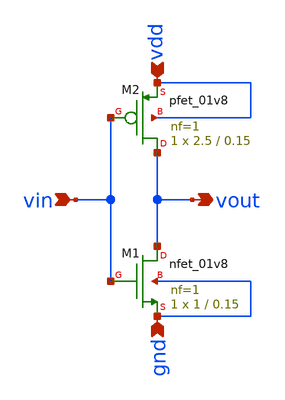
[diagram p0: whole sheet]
** sch_path: schematic/cmos_inverter.sch
**.subckt cmos_inverter vin vdd gnd vout
*.ipin vin
*.ipin vdd
*.ipin gnd
*.opin vout
XM1 vout vin gnd gnd sky130_fd_pr__nfet_01v8 L=0.15 W=1 nf=1 ad='int((1 + 1)/2) * 1 / 1 * 0.29' as='int((1 + 2)/2) * 1 / 1 * 0.29'
+ pd='2*int((1 + 1)/2) * (1 / 1 + 0.29)' ps='2*int((1 + 2)/2) * (1 / 1 + 0.29)' nrd='0.29 / 1 ' nrs='0.29 / 1 '
+ sa=0 sb=0 sd=0 mult=1 m=1
XM2 vout vin vdd vdd sky130_fd_pr__pfet_01v8 L=0.15 W=2.5 nf=1 ad='int((1 + 1)/2) * 2.5 / 1 * 0.29' as='int((1 + 2)/2) * 2.5 / 1 * 0.29'
+ pd='2*int((1 + 1)/2) * (2.5 / 1 + 0.29)' ps='2*int((1 + 2)/2) * (2.5 / 1 + 0.29)' nrd='0.29 / 2.5 ' nrs='0.29 / 2.5 '
+ sa=0 sb=0 sd=0 mult=1 m=1
**.ends
.end
